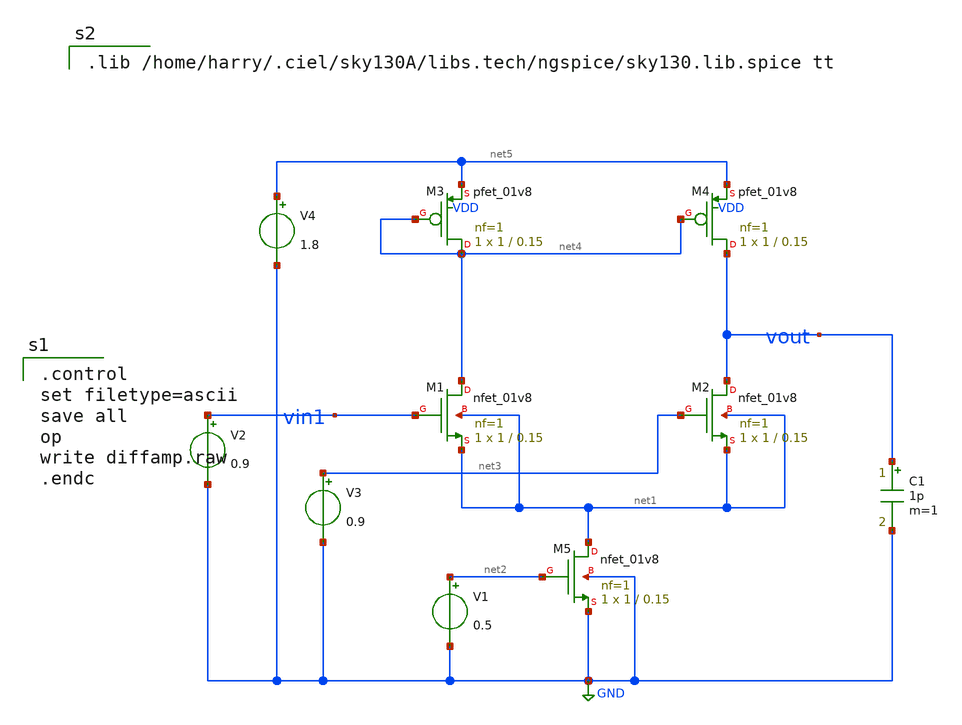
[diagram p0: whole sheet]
** sch_path: magic_xschem_ngspice/DiffAmpMirrorLoad.sch
**.subckt DiffAmpMirrorLoad
XM1 net4 vin1 net1 net1 sky130_fd_pr__nfet_01v8 L=0.15 W=1 nf=1 ad='int((1 + 1)/2) * 1 / 1 * 0.29' as='int((1 + 2)/2) * 1 / 1 * 0.29'
+ pd='2*int((1 + 1)/2) * (1 / 1 + 0.29)' ps='2*int((1 + 2)/2) * (1 / 1 + 0.29)' nrd='0.29 / 1 ' nrs='0.29 / 1 '
+ sa=0 sb=0 sd=0 mult=1 m=1
XM2 vout net3 net1 net1 sky130_fd_pr__nfet_01v8 L=0.15 W=1 nf=1 ad='int((1 + 1)/2) * 1 / 1 * 0.29' as='int((1 + 2)/2) * 1 / 1 * 0.29'
+ pd='2*int((1 + 1)/2) * (1 / 1 + 0.29)' ps='2*int((1 + 2)/2) * (1 / 1 + 0.29)' nrd='0.29 / 1 ' nrs='0.29 / 1 '
+ sa=0 sb=0 sd=0 mult=1 m=1
XM5 net1 net2 GND GND sky130_fd_pr__nfet_01v8 L=0.15 W=1 nf=1 ad='int((1 + 1)/2) * 1 / 1 * 0.29' as='int((1 + 2)/2) * 1 / 1 * 0.29'
+ pd='2*int((1 + 1)/2) * (1 / 1 + 0.29)' ps='2*int((1 + 2)/2) * (1 / 1 + 0.29)' nrd='0.29 / 1 ' nrs='0.29 / 1 '
+ sa=0 sb=0 sd=0 mult=1 m=1
V1 net2 GND 0.5
V2 vin1 GND 0.9
V3 net3 GND 0.9
V4 net5 GND 1.8
C1 vout GND 1p m=1
XM3 net4 net4 net5 VDD sky130_fd_pr__pfet_01v8 L=0.15 W=1 nf=1 ad='int((1 + 1)/2) * 1 / 1 * 0.29' as='int((1 + 2)/2) * 1 / 1 * 0.29'
+ pd='2*int((1 + 1)/2) * (1 / 1 + 0.29)' ps='2*int((1 + 2)/2) * (1 / 1 + 0.29)' nrd='0.29 / 1 ' nrs='0.29 / 1 '
+ sa=0 sb=0 sd=0 mult=1 m=1
XM4 vout net4 net5 VDD sky130_fd_pr__pfet_01v8 L=0.15 W=1 nf=1 ad='int((1 + 1)/2) * 1 / 1 * 0.29' as='int((1 + 2)/2) * 1 / 1 * 0.29'
+ pd='2*int((1 + 1)/2) * (1 / 1 + 0.29)' ps='2*int((1 + 2)/2) * (1 / 1 + 0.29)' nrd='0.29 / 1 ' nrs='0.29 / 1 '
+ sa=0 sb=0 sd=0 mult=1 m=1
**** begin user architecture code

.control
set filetype=ascii
save all
op
write diffamp.raw
.endc


.lib /home/harry/.ciel/sky130A/libs.tech/ngspice/sky130.lib.spice tt

**** end user architecture code
**.ends
.GLOBAL GND
.end
